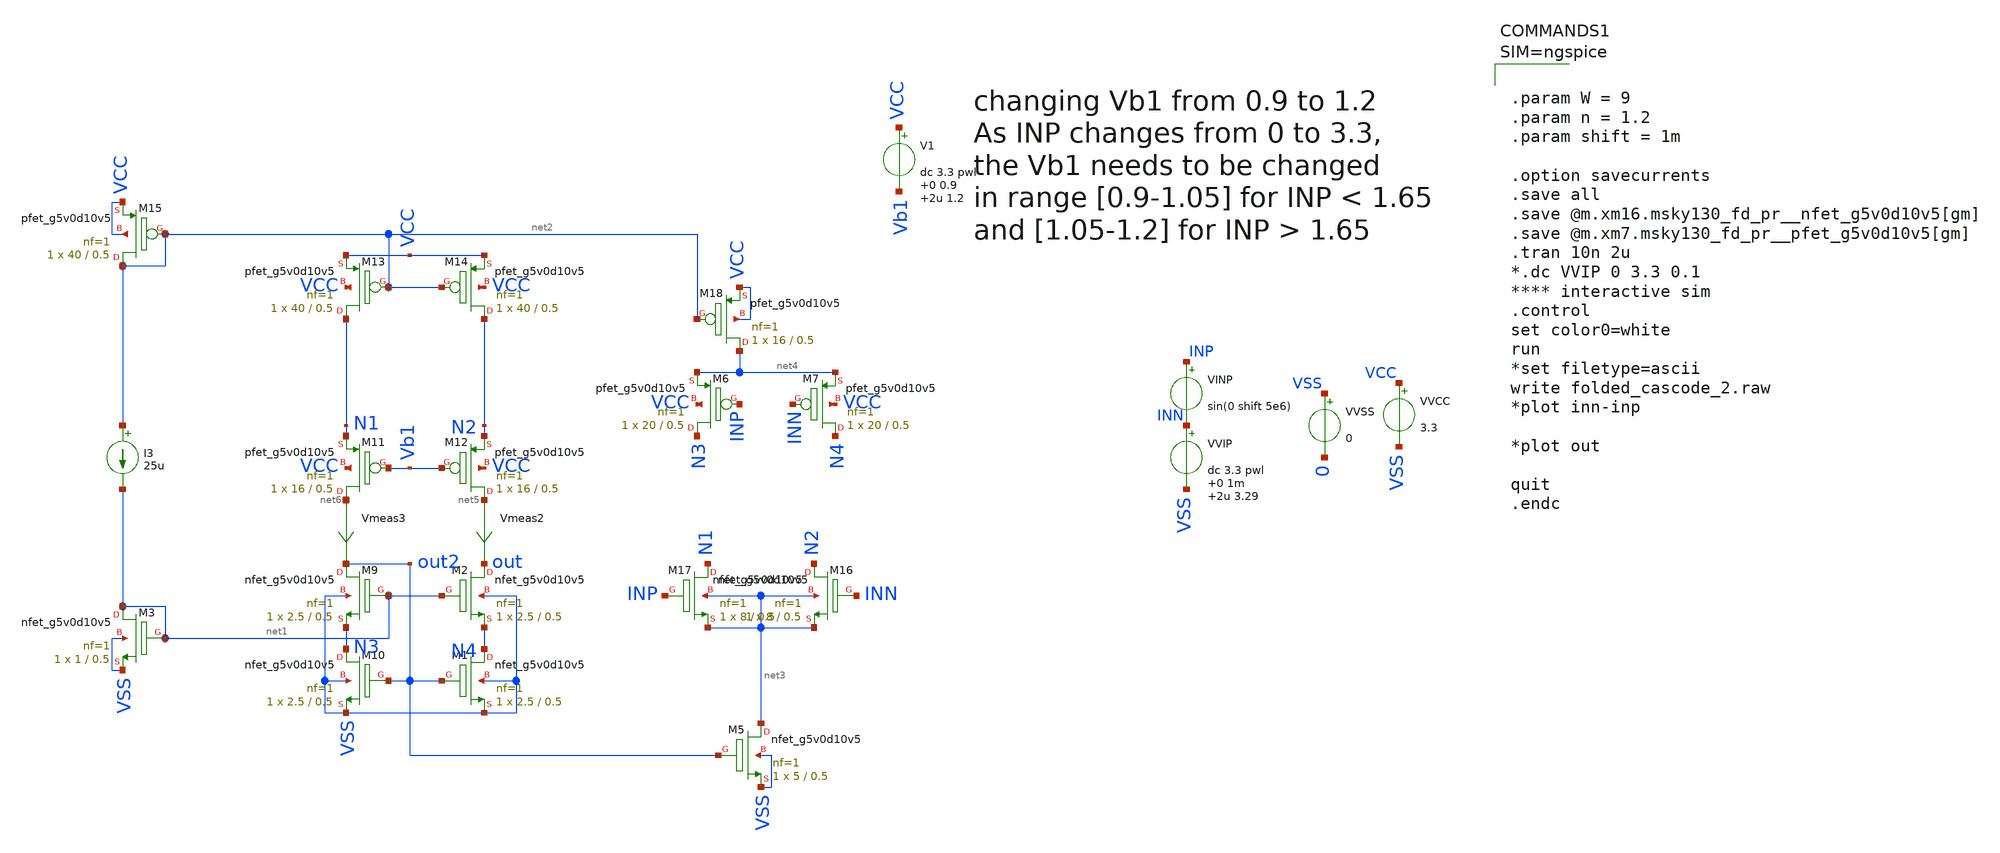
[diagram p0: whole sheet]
** sch_path: folded_cascode/folded_cascode_2.sch
.lib $::SKYWATER_MODELS/sky130.lib.spice.ss.red ss
.include $::SKYWATER_STDCELLS/sky130_fd_sc_hd.spice

**.subckt folded_cascode_2
VINP INP INN sin(0 shift 5e6)
VVSS VSS 0 0
VVCC VCC VSS 3.3
VVIP INN VSS dc 3.3 pwl 0 1m 2u 3.29

XM1 N4 out2 VSS VSS sky130_fd_pr__nfet_g5v0d10v5 L=0.5 W=2.5 nf=1 ad='int((nf+1)/2) * W/nf * 0.29' as='int((nf+2)/2) * W/nf * 0.29'
+ pd='2*int((nf+1)/2) * (W/nf + 0.29)' ps='2*int((nf+2)/2) * (W/nf + 0.29)' nrd='0.29 / W' nrs='0.29 / W'
+ sa=0 sb=0 sd=0 mult=1 m=1
XM2 out net1 N4 VSS sky130_fd_pr__nfet_g5v0d10v5 L=0.5 W=2.5 nf=1 ad='int((nf+1)/2) * W/nf * 0.29' as='int((nf+2)/2) * W/nf * 0.29'
+ pd='2*int((nf+1)/2) * (W/nf + 0.29)' ps='2*int((nf+2)/2) * (W/nf + 0.29)' nrd='0.29 / W' nrs='0.29 / W'
+ sa=0 sb=0 sd=0 mult=1 m=1
XM3 net1 net1 VSS VSS sky130_fd_pr__nfet_g5v0d10v5 L=0.5 W=1 nf=1 ad='int((nf+1)/2) * W/nf * 0.29' as='int((nf+2)/2) * W/nf * 0.29'
+ pd='2*int((nf+1)/2) * (W/nf + 0.29)' ps='2*int((nf+2)/2) * (W/nf + 0.29)' nrd='0.29 / W' nrs='0.29 / W'
+ sa=0 sb=0 sd=0 mult=1 m=1
XM9 out2 net1 N3 VSS sky130_fd_pr__nfet_g5v0d10v5 L=0.5 W=2.5 nf=1 ad='int((nf+1)/2) * W/nf * 0.29' as='int((nf+2)/2) * W/nf * 0.29'
+ pd='2*int((nf+1)/2) * (W/nf + 0.29)' ps='2*int((nf+2)/2) * (W/nf + 0.29)' nrd='0.29 / W' nrs='0.29 / W'
+ sa=0 sb=0 sd=0 mult=1 m=1
XM10 N3 out2 VSS VSS sky130_fd_pr__nfet_g5v0d10v5 L=0.5 W=2.5 nf=1 ad='int((nf+1)/2) * W/nf * 0.29' as='int((nf+2)/2) * W/nf * 0.29'
+ pd='2*int((nf+1)/2) * (W/nf + 0.29)' ps='2*int((nf+2)/2) * (W/nf + 0.29)' nrd='0.29 / W' nrs='0.29 / W'
+ sa=0 sb=0 sd=0 mult=1 m=1
Vmeas2 net5 out 0
.save i(vmeas2)
Vmeas3 net6 out2 0
.save i(vmeas3)
XM11 net6 Vb1 N1 VCC sky130_fd_pr__pfet_g5v0d10v5 L=0.5 W=16 nf=1 ad='int((nf+1)/2) * W/nf * 0.29' as='int((nf+2)/2) * W/nf * 0.29'
+ pd='2*int((nf+1)/2) * (W/nf + 0.29)' ps='2*int((nf+2)/2) * (W/nf + 0.29)' nrd='0.29 / W' nrs='0.29 / W'
+ sa=0 sb=0 sd=0 mult=1 m=1
XM12 net5 Vb1 N2 VCC sky130_fd_pr__pfet_g5v0d10v5 L=0.5 W=16 nf=1 ad='int((nf+1)/2) * W/nf * 0.29' as='int((nf+2)/2) * W/nf * 0.29'
+ pd='2*int((nf+1)/2) * (W/nf + 0.29)' ps='2*int((nf+2)/2) * (W/nf + 0.29)' nrd='0.29 / W' nrs='0.29 / W'
+ sa=0 sb=0 sd=0 mult=1 m=1
XM13 N1 net2 VCC VCC sky130_fd_pr__pfet_g5v0d10v5 L=0.5 W=40 nf=1 ad='int((nf+1)/2) * W/nf * 0.29' as='int((nf+2)/2) * W/nf * 0.29'
+ pd='2*int((nf+1)/2) * (W/nf + 0.29)' ps='2*int((nf+2)/2) * (W/nf + 0.29)' nrd='0.29 / W' nrs='0.29 / W'
+ sa=0 sb=0 sd=0 mult=1 m=1
XM14 N2 net2 VCC VCC sky130_fd_pr__pfet_g5v0d10v5 L=0.5 W=40 nf=1 ad='int((nf+1)/2) * W/nf * 0.29' as='int((nf+2)/2) * W/nf * 0.29'
+ pd='2*int((nf+1)/2) * (W/nf + 0.29)' ps='2*int((nf+2)/2) * (W/nf + 0.29)' nrd='0.29 / W' nrs='0.29 / W'
+ sa=0 sb=0 sd=0 mult=1 m=1
XM15 net2 net2 VCC VCC sky130_fd_pr__pfet_g5v0d10v5 L=0.5 W=40 nf=1 ad='int((nf+1)/2) * W/nf * 0.29'
+ as='int((nf+2)/2) * W/nf * 0.29' pd='2*int((nf+1)/2) * (W/nf + 0.29)' ps='2*int((nf+2)/2) * (W/nf + 0.29)'
+ nrd='0.29 / W' nrs='0.29 / W' sa=0 sb=0 sd=0 mult=1 m=1
I3 net2 net1 25u
XM16 N2 INN net3 net3 sky130_fd_pr__nfet_g5v0d10v5 L=0.5 W=8 nf=1 ad='int((nf+1)/2) * W/nf * 0.29' as='int((nf+2)/2) * W/nf * 0.29'
+ pd='2*int((nf+1)/2) * (W/nf + 0.29)' ps='2*int((nf+2)/2) * (W/nf + 0.29)' nrd='0.29 / W' nrs='0.29 / W'
+ sa=0 sb=0 sd=0 mult=1 m=1
XM17 N1 INP net3 net3 sky130_fd_pr__nfet_g5v0d10v5 L=0.5 W=8 nf=1 ad='int((nf+1)/2) * W/nf * 0.29' as='int((nf+2)/2) * W/nf * 0.29'
+ pd='2*int((nf+1)/2) * (W/nf + 0.29)' ps='2*int((nf+2)/2) * (W/nf + 0.29)' nrd='0.29 / W' nrs='0.29 / W'
+ sa=0 sb=0 sd=0 mult=1 m=1
V1 VCC Vb1 dc 3.3 pwl 0 0.9 2u 1.2

XM5 net3 out2 VSS VSS sky130_fd_pr__nfet_g5v0d10v5 L=0.5 W=5 nf=1 ad='int((nf+1)/2) * W/nf * 0.29' as='int((nf+2)/2) * W/nf * 0.29'
+ pd='2*int((nf+1)/2) * (W/nf + 0.29)' ps='2*int((nf+2)/2) * (W/nf + 0.29)' nrd='0.29 / W' nrs='0.29 / W'
+ sa=0 sb=0 sd=0 mult=1 m=1
XM6 N3 INP net4 VCC sky130_fd_pr__pfet_g5v0d10v5 L=0.5 W=20 nf=1 ad='int((nf+1)/2) * W/nf * 0.29' as='int((nf+2)/2) * W/nf * 0.29'
+ pd='2*int((nf+1)/2) * (W/nf + 0.29)' ps='2*int((nf+2)/2) * (W/nf + 0.29)' nrd='0.29 / W' nrs='0.29 / W'
+ sa=0 sb=0 sd=0 mult=1 m=1
XM7 N4 INN net4 VCC sky130_fd_pr__pfet_g5v0d10v5 L=0.5 W=20 nf=1 ad='int((nf+1)/2) * W/nf * 0.29' as='int((nf+2)/2) * W/nf * 0.29'
+ pd='2*int((nf+1)/2) * (W/nf + 0.29)' ps='2*int((nf+2)/2) * (W/nf + 0.29)' nrd='0.29 / W' nrs='0.29 / W'
+ sa=0 sb=0 sd=0 mult=1 m=1
XM18 net4 net2 VCC VCC sky130_fd_pr__pfet_g5v0d10v5 L=0.5 W=16 nf=1 ad='int((nf+1)/2) * W/nf * 0.29'
+ as='int((nf+2)/2) * W/nf * 0.29' pd='2*int((nf+1)/2) * (W/nf + 0.29)' ps='2*int((nf+2)/2) * (W/nf + 0.29)'
+ nrd='0.29 / W' nrs='0.29 / W' sa=0 sb=0 sd=0 mult=1 m=1
**** begin user architecture code



.param W = 9
.param n = 1.2
.param shift = 1m

.option savecurrents
.save all
.save @m.xm16.msky130_fd_pr__nfet_g5v0d10v5[gm]
.save @m.xm7.msky130_fd_pr__pfet_g5v0d10v5[gm]
.tran 10n 2u
*.dc VVIP 0 3.3 0.1
**** interactive sim
.control
set color0=white
run
*set filetype=ascii
write folded_cascode_2.raw
*plot inn-inp

*plot out

quit
.endc



**** end user architecture code
**.ends
.end
